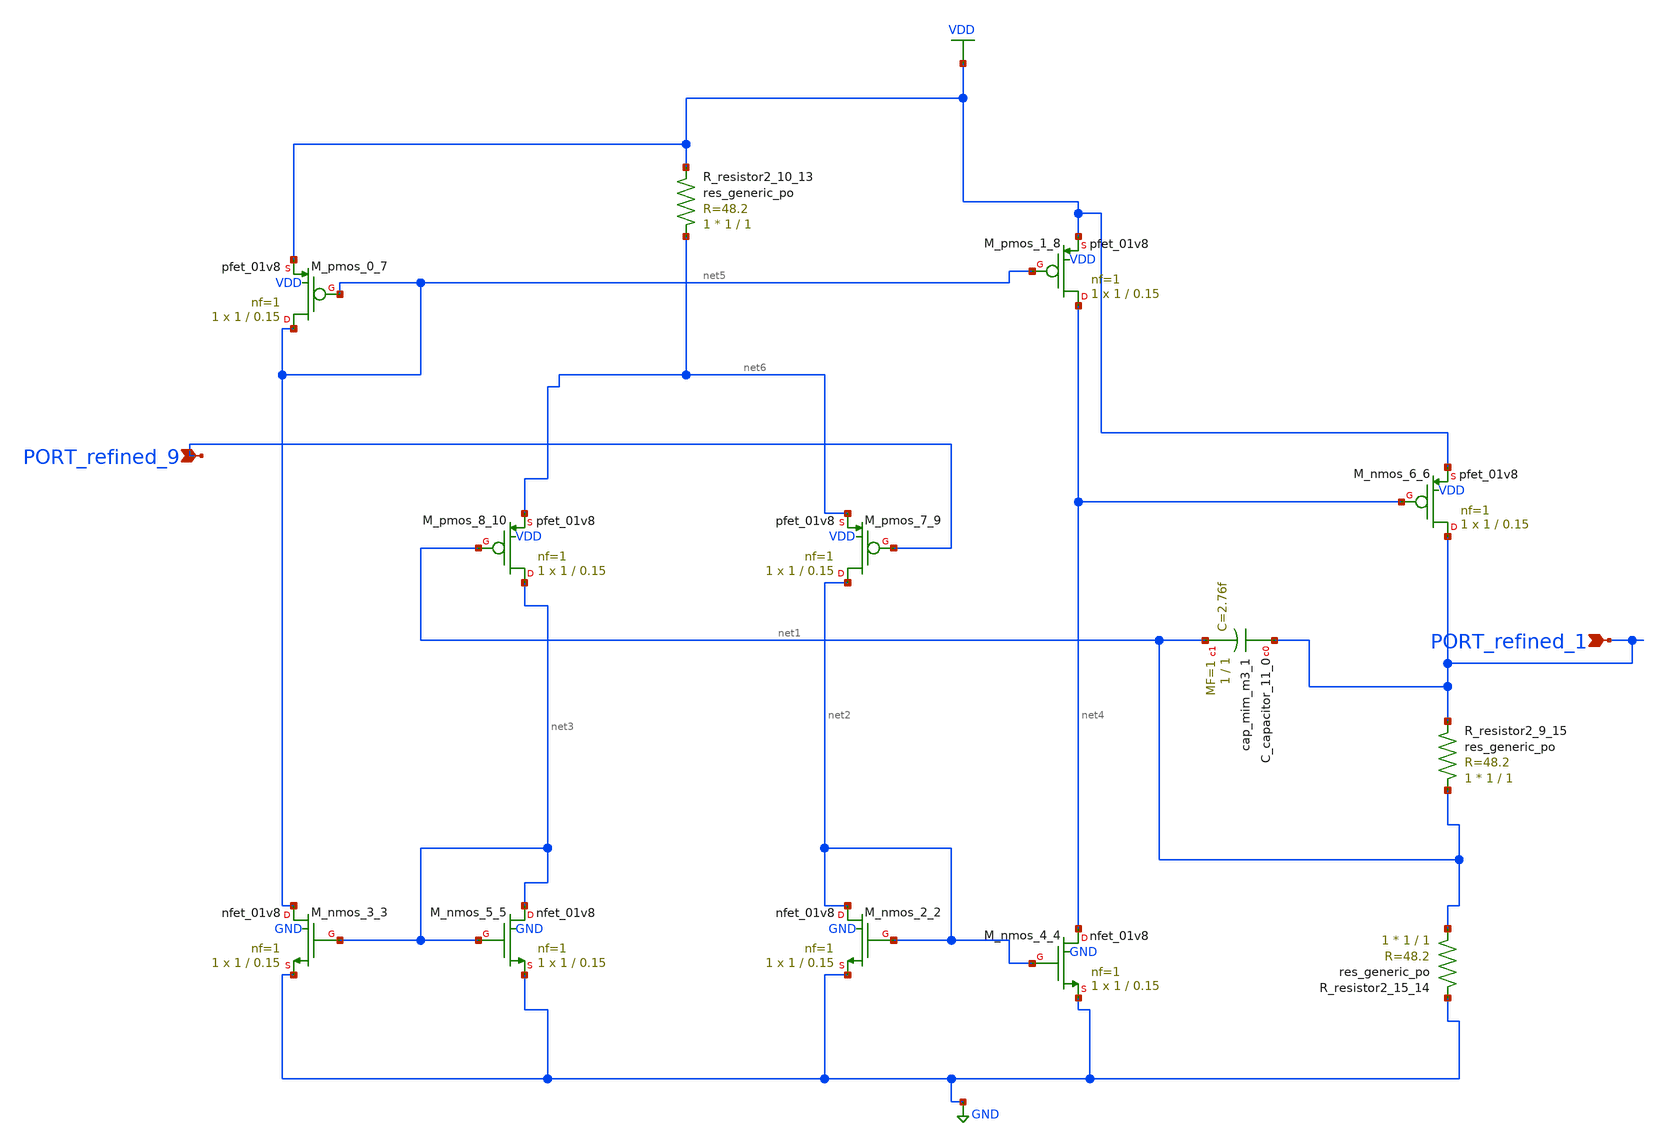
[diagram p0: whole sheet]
** sch_path: schematics/SchemGen/10_1007_s00502-020-00859-w_04_001_crop1.sch
**.subckt 10_1007_s00502-020-00859-w_04_001_crop1 PORT_refined_1 PORT_refined_9
*.ipin PORT_refined_1
*.ipin PORT_refined_9
XC_capacitor_11_0 PORT_refined_1 net1 sky130_fd_pr__cap_mim_m3_1 W=1 L=1 MF=1 m=1
XM_nmos_2_2 net2 net2 GND GND sky130_fd_pr__nfet_01v8 L=0.15 W=1 nf=1 ad='int((1 + 1)/2) * 1 / 1 * 0.29'
+ as='int((1 + 2)/2) * 1 / 1 * 0.29' pd='2*int((1 + 1)/2) * (1 / 1 + 0.29)' ps='2*int((1 + 2)/2) * (1 / 1 + 0.29)'
+ nrd='0.29 / 1 ' nrs='0.29 / 1 ' sa=0 sb=0 sd=0 mult=1 m=1
XM_nmos_3_3 net5 net3 GND GND sky130_fd_pr__nfet_01v8 L=0.15 W=1 nf=1 ad='int((1 + 1)/2) * 1 / 1 * 0.29'
+ as='int((1 + 2)/2) * 1 / 1 * 0.29' pd='2*int((1 + 1)/2) * (1 / 1 + 0.29)' ps='2*int((1 + 2)/2) * (1 / 1 + 0.29)'
+ nrd='0.29 / 1 ' nrs='0.29 / 1 ' sa=0 sb=0 sd=0 mult=1 m=1
XM_nmos_4_4 net4 net2 GND GND sky130_fd_pr__nfet_01v8 L=0.15 W=1 nf=1 ad='int((1 + 1)/2) * 1 / 1 * 0.29'
+ as='int((1 + 2)/2) * 1 / 1 * 0.29' pd='2*int((1 + 1)/2) * (1 / 1 + 0.29)' ps='2*int((1 + 2)/2) * (1 / 1 + 0.29)'
+ nrd='0.29 / 1 ' nrs='0.29 / 1 ' sa=0 sb=0 sd=0 mult=1 m=1
XM_nmos_5_5 net3 net3 GND GND sky130_fd_pr__nfet_01v8 L=0.15 W=1 nf=1 ad='int((1 + 1)/2) * 1 / 1 * 0.29'
+ as='int((1 + 2)/2) * 1 / 1 * 0.29' pd='2*int((1 + 1)/2) * (1 / 1 + 0.29)' ps='2*int((1 + 2)/2) * (1 / 1 + 0.29)'
+ nrd='0.29 / 1 ' nrs='0.29 / 1 ' sa=0 sb=0 sd=0 mult=1 m=1
XM_nmos_6_6 PORT_refined_1 net4 VDD VDD sky130_fd_pr__pfet_01v8 L=0.15 W=1 nf=1 ad='int((1 + 1)/2) * 1 / 1 * 0.29'
+ as='int((1 + 2)/2) * 1 / 1 * 0.29' pd='2*int((1 + 1)/2) * (1 / 1 + 0.29)' ps='2*int((1 + 2)/2) * (1 / 1 + 0.29)'
+ nrd='0.29 / 1 ' nrs='0.29 / 1 ' sa=0 sb=0 sd=0 mult=1 m=1
XM_pmos_0_7 net5 net5 VDD VDD sky130_fd_pr__pfet_01v8 L=0.15 W=1 nf=1 ad='int((1 + 1)/2) * 1 / 1 * 0.29'
+ as='int((1 + 2)/2) * 1 / 1 * 0.29' pd='2*int((1 + 1)/2) * (1 / 1 + 0.29)' ps='2*int((1 + 2)/2) * (1 / 1 + 0.29)'
+ nrd='0.29 / 1 ' nrs='0.29 / 1 ' sa=0 sb=0 sd=0 mult=1 m=1
XM_pmos_1_8 net4 net5 VDD VDD sky130_fd_pr__pfet_01v8 L=0.15 W=1 nf=1 ad='int((1 + 1)/2) * 1 / 1 * 0.29'
+ as='int((1 + 2)/2) * 1 / 1 * 0.29' pd='2*int((1 + 1)/2) * (1 / 1 + 0.29)' ps='2*int((1 + 2)/2) * (1 / 1 + 0.29)'
+ nrd='0.29 / 1 ' nrs='0.29 / 1 ' sa=0 sb=0 sd=0 mult=1 m=1
XM_pmos_7_9 net2 PORT_refined_9 net6 VDD sky130_fd_pr__pfet_01v8 L=0.15 W=1 nf=1 ad='int((1 + 1)/2) * 1 / 1 * 0.29'
+ as='int((1 + 2)/2) * 1 / 1 * 0.29' pd='2*int((1 + 1)/2) * (1 / 1 + 0.29)' ps='2*int((1 + 2)/2) * (1 / 1 + 0.29)'
+ nrd='0.29 / 1 ' nrs='0.29 / 1 ' sa=0 sb=0 sd=0 mult=1 m=1
XM_pmos_8_10 net3 net1 net6 VDD sky130_fd_pr__pfet_01v8 L=0.15 W=1 nf=1 ad='int((1 + 1)/2) * 1 / 1 * 0.29'
+ as='int((1 + 2)/2) * 1 / 1 * 0.29' pd='2*int((1 + 1)/2) * (1 / 1 + 0.29)' ps='2*int((1 + 2)/2) * (1 / 1 + 0.29)'
+ nrd='0.29 / 1 ' nrs='0.29 / 1 ' sa=0 sb=0 sd=0 mult=1 m=1
XR_resistor2_10_13 net6 VDD sky130_fd_pr__res_generic_po W=1 L=1 m=1
XR_resistor2_15_14 net1 GND sky130_fd_pr__res_generic_po W=1 L=1 m=1
XR_resistor2_9_15 net1 PORT_refined_1 sky130_fd_pr__res_generic_po W=1 L=1 m=1
**.ends
.GLOBAL GND
.GLOBAL VDD
.end
